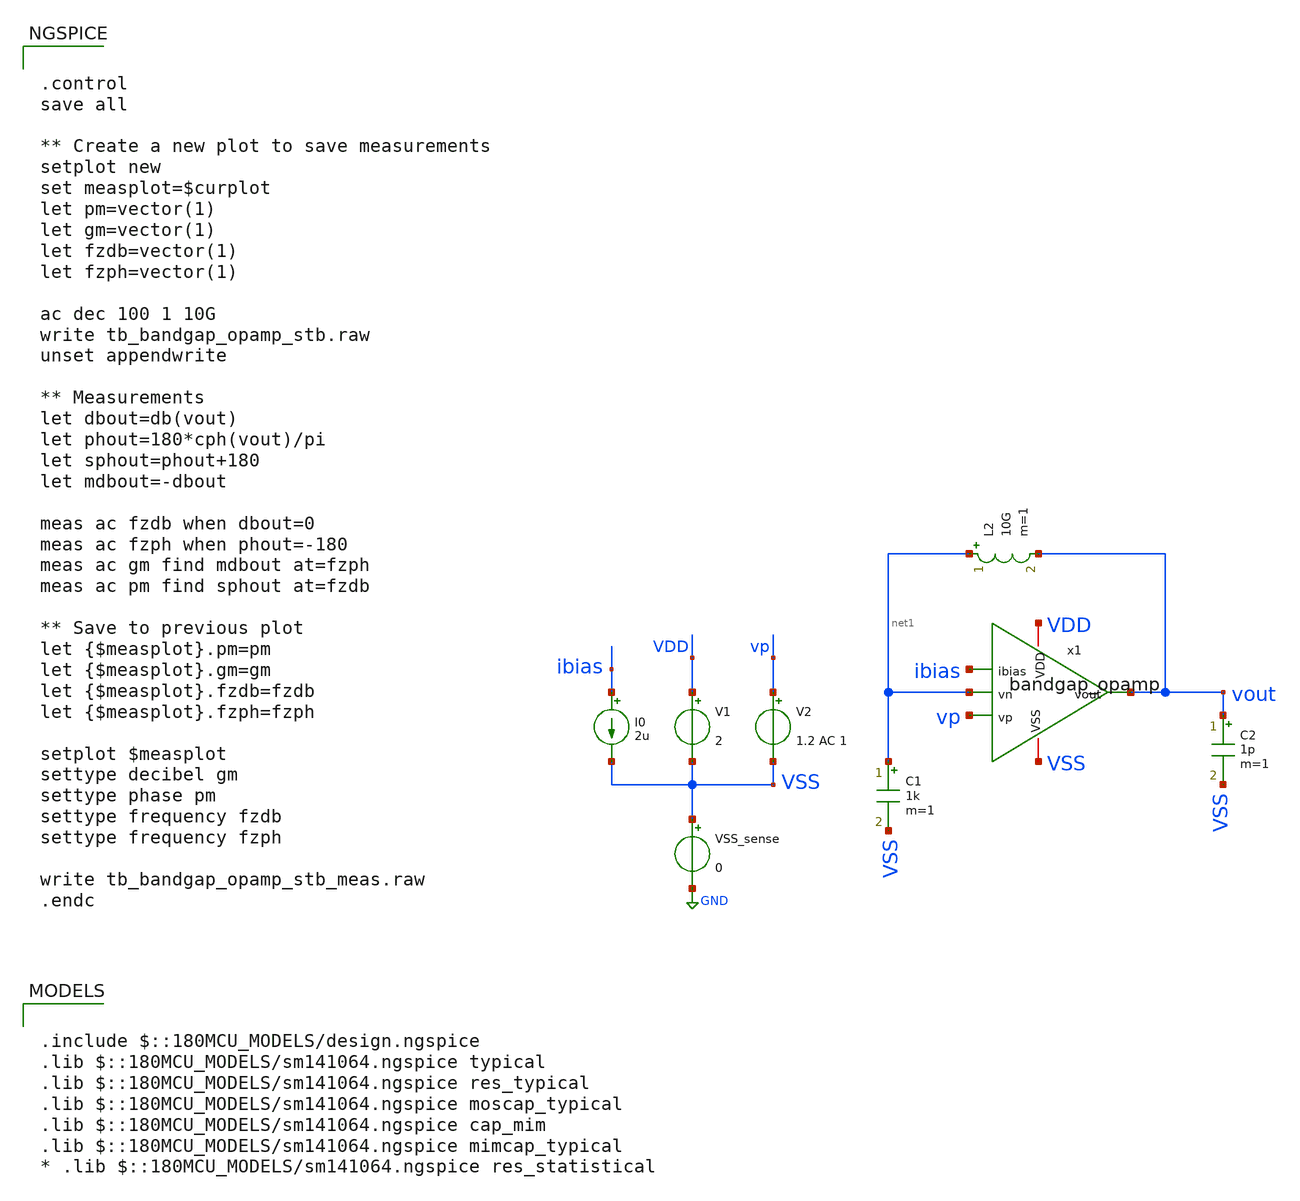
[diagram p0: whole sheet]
** sch_path: designs/libs/tb_bandgap/tb_bandgap_opamp_stb/tb_bandgap_opamp_stb.sch
**.subckt tb_bandgap_opamp_stb
C1 net1 VSS 1k m=1
V1 VDD VSS 2
V2 vp VSS 1.2 AC 1
VSS_sense VSS GND 0
C2 vout VSS 1p m=1
L2 net1 vout 10G m=1
I0 ibias VSS 2u
x1 VDD ibias net1 vp vout VSS bandgap_opamp
**** begin user architecture code

.include $::180MCU_MODELS/design.ngspice
.lib $::180MCU_MODELS/sm141064.ngspice typical
.lib $::180MCU_MODELS/sm141064.ngspice res_typical
.lib $::180MCU_MODELS/sm141064.ngspice moscap_typical
.lib $::180MCU_MODELS/sm141064.ngspice cap_mim
.lib $::180MCU_MODELS/sm141064.ngspice mimcap_typical
* .lib $::180MCU_MODELS/sm141064.ngspice res_statistical



.control
save all

** Create a new plot to save measurements
setplot new
set measplot=$curplot
let pm=vector(1)
let gm=vector(1)
let fzdb=vector(1)
let fzph=vector(1)

ac dec 100 1 10G
write tb_bandgap_opamp_stb.raw
unset appendwrite

** Measurements
let dbout=db(vout)
let phout=180*cph(vout)/pi
let sphout=phout+180
let mdbout=-dbout

meas ac fzdb when dbout=0
meas ac fzph when phout=-180
meas ac gm find mdbout at=fzph
meas ac pm find sphout at=fzdb

** Save to previous plot
let {$measplot}.pm=pm
let {$measplot}.gm=gm
let {$measplot}.fzdb=fzdb
let {$measplot}.fzph=fzph

setplot $measplot
settype decibel gm
settype phase pm
settype frequency fzdb
settype frequency fzph

write tb_bandgap_opamp_stb_meas.raw
.endc


**** end user architecture code
**.ends
.GLOBAL GND
.end
